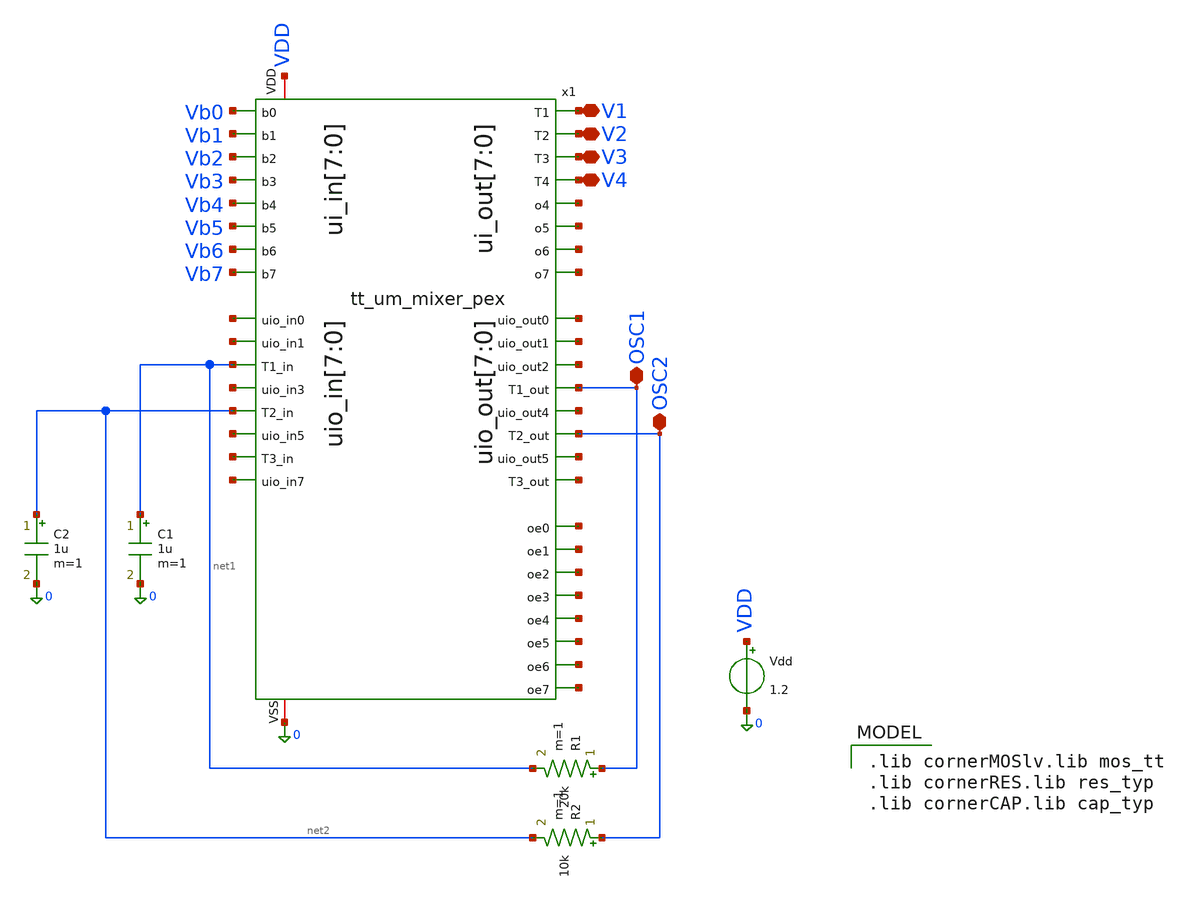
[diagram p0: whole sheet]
** sch_path: xschem/tt_um_mixer_tb.sch
**.subckt tt_um_mixer_tb V1 V2 V3 V4 OSC1 OSC2
*.iopin V1
*.iopin V2
*.iopin V3
*.iopin V4
*.iopin OSC1
*.iopin OSC2
Vdd VDD 0 1.2

.include ../../mag/tt_um_nikleberg_mixer.pex.spice
x1 VDD 0 net3 net4 net5 net6 net7 net8 net9 net1 net10 net11 OSC2 OSC1 net12 net13 net2 net14 net15
+ net16 net17 net18 net19 net20 Vb0 net21 Vb1 Vb2 Vb3 Vb4 Vb5 Vb6 Vb7 V4 V3 V2 V1 net22 net23 net24 net25
+ net26 tt_um_nikleberg_mixer

C1 net1 0 1u m=1
R1 OSC1 net1 20k m=1
C2 net2 0 1u m=1
R2 OSC2 net2 10k m=1
**** begin user architecture code
 .lib cornerMOSlv.lib mos_tt
.lib cornerRES.lib res_typ
.lib cornerCAP.lib cap_typ



.param temp=27
.option method=gear
.include 8bit_triangle.spice
.control
op
write tt_um_mixer_tb.raw
set appendwrite
reset
save all
tran 200ns 4ms
write tt_um_mixer_tb.raw
quit 0
.endc


**** end user architecture code
**.ends
.end
